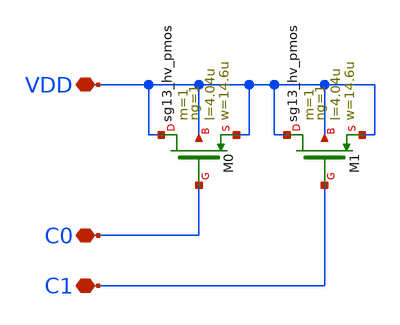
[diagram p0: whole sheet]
** sch_path: xschem/dacbuffer_1chan.sch
**.subckt dacbuffer_1chan VDD C0 C1
*.iopin VDD
*.iopin C0
*.iopin C1
XM1 VDD C1 VDD VDD sg13_hv_pmos w=14.6u l=4.04u ng=1 m=1 mm_ok=1
XM0 VDD C0 VDD VDD sg13_hv_pmos w=14.6u l=4.04u ng=1 m=1 mm_ok=1
**.ends
.end
